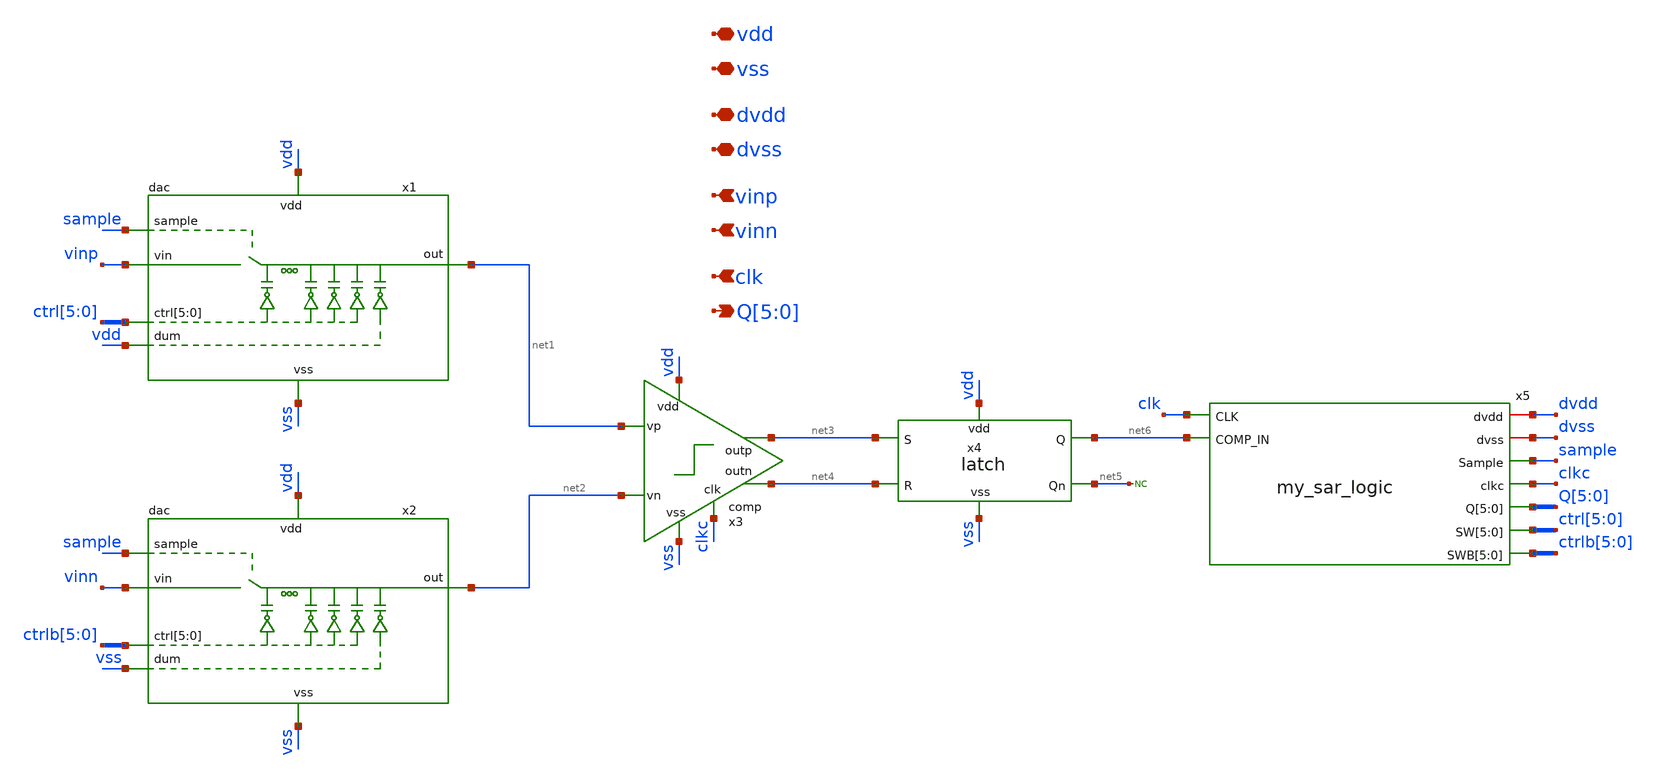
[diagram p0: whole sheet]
** sch_path: xschem/adc/6bit_saradc.sch
**.subckt 6bit_saradc vdd vss dvdd dvss vinp vinn clk Q[5],Q[4],Q[3],Q[2],Q[1],Q[0]
*.iopin vdd
*.iopin vss
*.iopin dvdd
*.iopin dvss
*.ipin vinp
*.ipin vinn
*.ipin clk
*.opin Q[5],Q[4],Q[3],Q[2],Q[1],Q[0]
x3 vss vdd clkc net3 net1 net4 net2 comp
x4 vdd net6 net5 vss net4 net3 latch
* noconn #net5
x5 dvdd dvss clk net6 sample clkc Q[5] Q[4] Q[3] Q[2] Q[1] Q[0] ctrl[5] ctrl[4] ctrl[3] ctrl[2]
+ ctrl[1] ctrl[0] ctrlb[5] ctrlb[4] ctrlb[3] ctrlb[2] ctrlb[1] ctrlb[0] my_sar_logic
x1 net1 sample vdd vss vinp ctrl[5] ctrl[4] ctrl[3] ctrl[2] ctrl[1] ctrl[0] vdd dac
x2 net2 sample vdd vss vinn ctrlb[5] ctrlb[4] ctrlb[3] ctrlb[2] ctrlb[1] ctrlb[0] vss dac
**.ends
.end
